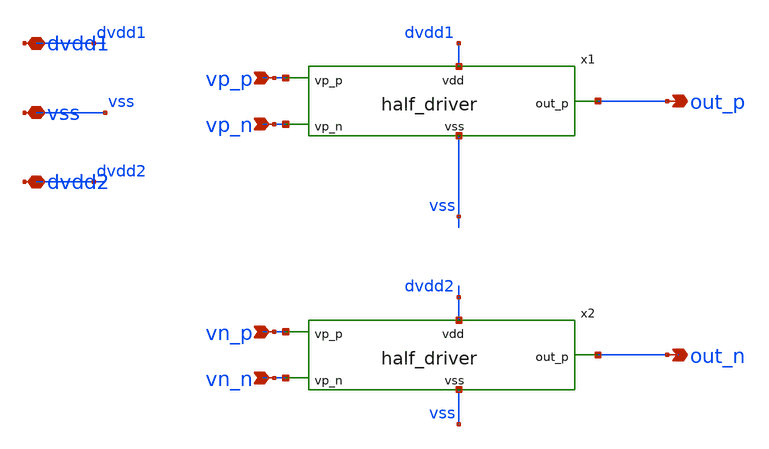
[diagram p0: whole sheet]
** sch_path: xschem/src/output_driver/output_driver.sch
**.subckt output_driver vp_p vp_n vn_p vn_n out_p out_n dvdd1 vss dvdd2
*.ipin vp_p
*.ipin vp_n
*.ipin vn_p
*.ipin vn_n
*.opin out_p
*.opin out_n
*.iopin dvdd1
*.iopin vss
*.iopin dvdd2
x1 dvdd1 vss vp_p out_p vp_n half_driver
x2 dvdd2 vss vn_p out_n vn_n half_driver
**.ends

* expanding   symbol:  src/output_driver/half_driver.sym # of pins=5
** sym_path: xschem/src/output_driver/half_driver.sym
** sch_path: xschem/src/output_driver/half_driver.sch
.subckt half_driver vdd vss vp_p out_p vp_n
*.ipin vp_p
*.ipin vp_n
*.opin out_p
*.iopin vdd
*.iopin vss
XM1 out_p vp_p vdd vdd sky130_fd_pr__pfet_01v8 L=0.15 W=12000 nf=200 ad='int((nf+1)/2) * W/nf * 0.29'
+ as='int((nf+2)/2) * W/nf * 0.29' pd='2*int((nf+1)/2) * (W/nf + 0.29)' ps='2*int((nf+2)/2) * (W/nf + 0.29)'
+ nrd='0.29 / W' nrs='0.29 / W' sa=0 sb=0 sd=0 mult=1 m=1
XM2 out_p vp_n vss vss sky130_fd_pr__nfet_01v8 L=0.15 W=2400 nf=100 ad='int((nf+1)/2) * W/nf * 0.29'
+ as='int((nf+2)/2) * W/nf * 0.29' pd='2*int((nf+1)/2) * (W/nf + 0.29)' ps='2*int((nf+2)/2) * (W/nf + 0.29)'
+ nrd='0.29 / W' nrs='0.29 / W' sa=0 sb=0 sd=0 mult=1 m=1
.ends

.end
